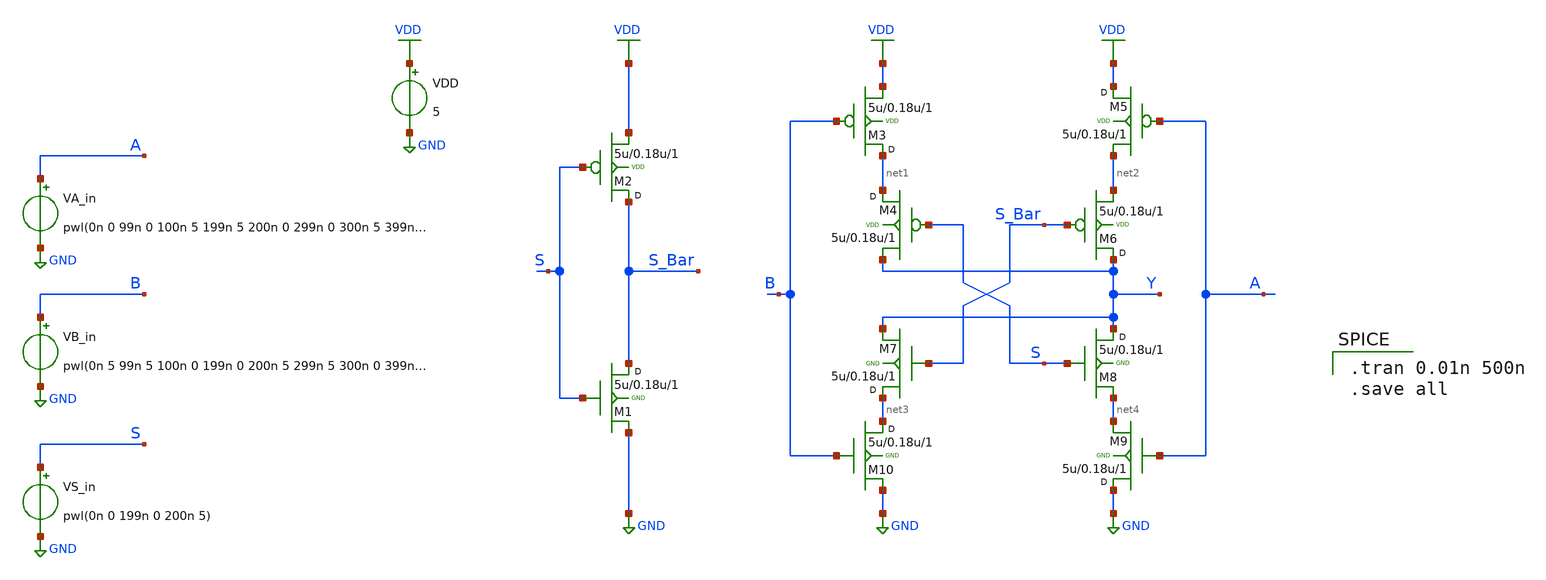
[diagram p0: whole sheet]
** sch_path: sch/MUX2X1_size_diff.sch
**.subckt MUX2X1_size_diff
M1 S_Bar S GND GND nfet w=5u l=0.18u m=1
M2 S_Bar S VDD VDD pfet w=5u l=0.18u m=1
M3 net1 B VDD VDD pfet w=5u l=0.18u m=1
M4 net1 S Y VDD pfet w=5u l=0.18u m=1
M5 VDD A net2 VDD pfet w=5u l=0.18u m=1
M6 Y S_Bar net2 VDD pfet w=5u l=0.18u m=1
M7 net3 S_Bar Y GND nfet w=5u l=0.18u m=1
M8 Y S net4 GND nfet w=5u l=0.18u m=1
M9 GND A net4 GND nfet w=5u l=0.18u m=1
M10 net3 B GND GND nfet w=5u l=0.18u m=1
VDD VDD GND 5
VA_in A GND pwl(0n 0 99n 0 100n 5 199n 5 200n 0 299n 0 300n 5 399n 5 400n 0)
VB_in B GND pwl(0n 5 99n 5 100n 0 199n 0 200n 5 299n 5 300n 0 399n 0 400n 5)
VS_in S GND pwl(0n 0 199n 0 200n 5)
**** begin user architecture code

.option wnflag=1
.MODEL nfet NMOS ( LEVEL   = 49 VERSION = 3.1            TNOM    = 27             TOX     = 1.4E-8
+ XJ      = 1.5E-7         NCH     = 1.7E17         VTH0    = 0.6484638 K1      = 0.8874212      K2
+      = -0.0978537     K3      = 24.0034885 K3B     = -7.2553705     W0      = 1.268969E-8    NLX     =
+ 1E-9 DVT0W   = 0              DVT1W   = 0              DVT2W   = 0 DVT0    = 3.8899304      DVT1    =
+ 0.4295545      DVT2    = -0.0862625 U0      = 454.7269155    UA      = 1E-13          UB      = 1.362113E-18
+ UC      = 1.430811E-11   VSAT    = 1.629926E5     A0      = 0.6165742 AGS     = 0.1163052      B0
+      = 2.433887E-6    B1      = 5E-6 KETA    = -2.051055E-3   A1      = 6.710587E-5    A2      = 0.37115
+ RDSW    = 1.342046E3     PRWG    = 0.0525473      PRWB    = 0.0422162 WR      = 1              WINT    =
+ 2.317656E-7    LINT    = 3.438422E-8 XL      = 0              XW      = 0              DWG     = -1.197811E-8
+ DWB     = 6.032429E-8    VOFF    = 0              NFACTOR = 0.684939 CIT     = 0              CDSC    =
+ 2.4E-4         CDSCD   = 0 CDSCB   = 0              ETA0    = 0.0323024      ETAB    = -1.472177E-3 DSUB
+    = 0.2796903      PCLM    = 2.5557332      PDIBLC1 = -0.2401157 PDIBLC2 = 2.505188E-3    PDIBLCB =
+ -0.0520225     DROUT   = 0.5945619 PSCBE1  = 5.499244E8     PSCBE2  = 4.527916E-5    PVAG    = 0 DELTA   =
+ 0.01           RSH     = 80.3           MOBMOD  = 1 PRT     = 0              UTE     = -1.5
+           KT1     = -0.11 KT1L    = 0              KT2     = 0.022          UA1     = 4.31E-9 UB1     = -7.61E-18
+      UC1     = -5.6E-11       AT      = 3.3E4 WL      = 0              WLN     = 1              WW      = 0
+ WWN     = 1              WWL     = 0              LL      = 0 LLN     = 1              LW      = 0
+              LWN     = 1 LWL     = 0              CAPMOD  = 2              XPART   = 0.5 CGDO    = 2.1E-10
+        CGSO    = 2.1E-10        CGBO    = 1E-9 CJ      = 4.156656E-4    PB      = 0.99           MJ      =
+ 0.4479288 CJSW    = 3.399348E-10   PBSW    = 0.1            MJSW    = 0.1142026 CJSWG   = 1.64E-10
+       PBSWG   = 0.1            MJSWG   = 0.1142026 CF      = 0              PVTH0   = 0.0959658      PRDSW   =
+ 103.9415756 PK2     = -0.034767      WKETA   = -0.0168116     LKETA   = 1.239789E-3     )


.MODEL pfet PMOS ( LEVEL   = 49 VERSION = 3.1            TNOM    = 27             TOX     = 1.4E-8
+ XJ      = 1.5E-7         NCH     = 1.7E17         VTH0    = -0.9500724 K1      = 0.5456507      K2
+      = 0.0105576      K3      = 4.5052654 K3B     = -0.931974      W0      = 1.127003E-7    NLX     =
+ 3.819935E-8 DVT0W   = 0              DVT1W   = 0              DVT2W   = 0 DVT0    = 2.7369297      DVT1    =
+ 0.4803414      DVT2    = -0.0786477 U0      = 212.1726489    UA      = 2.800492E-9    UB      = 1.059959E-21
+ UC      = -6.21265E-11   VSAT    = 2E5            A0      = 0.894794 AGS     = 0.1277092      B0
+      = 5.079049E-7    B1      = 5E-6 KETA    = -1.969136E-3   A1      = 0              A2      = 0.3 RDSW
+    = 2.51727E3      PRWG    = -3.93537E-3    PRWB    = -6.474415E-3 WR      = 1              WINT    =
+ 2.846891E-7    LINT    = 5.207504E-8 XL      = 0              XW      = 0              DWG     = -1.894994E-8
+ DWB     = 1.793161E-8    VOFF    = -0.0589646     NFACTOR = 0.9229882 CIT     = 0              CDSC
+    = 2.4E-4         CDSCD   = 0 CDSCB   = 0              ETA0    = 0.3701754      ETAB    = -0.0747353
+ DSUB    = 1              PCLM    = 2.0661973      PDIBLC1 = 0.0491197 PDIBLC2 = 4.022205E-3    PDIBLCB =
+ -0.0622551     DROUT   = 0.2243213 PSCBE1  = 5.126179E9     PSCBE2  = 5.004119E-10   PVAG    = 0.0167107 DELTA
+   = 0.01           RSH     = 101.7          MOBMOD  = 1 PRT     = 0              UTE     = -1.5
+           KT1     = -0.11 KT1L    = 0              KT2     = 0.022          UA1     = 4.31E-9 UB1     = -7.61E-18
+      UC1     = -5.6E-11       AT      = 3.3E4 WL      = 0              WLN     = 1              WW      = 0
+ WWN     = 1              WWL     = 0              LL      = 0 LLN     = 1              LW      = 0
+              LWN     = 1 LWL     = 0              CAPMOD  = 2              XPART   = 0.5 CGDO    = 2.89E-10
+       CGSO    = 2.89E-10       CGBO    = 1E-9 CJ      = 7.264536E-4    PB      = 0.9566163      MJ      =
+ 0.4977596 CJSW    = 2.873502E-10   PBSW    = 0.99           MJSW    = 0.3106308 CJSWG   = 6.4E-11
+        PBSWG   = 0.99           MJSWG   = 0.3106308 CF      = 0              PVTH0   = 5.98016E-3     PRDSW   =
+ 14.8598424 PK2     = 3.73981E-3     WKETA   = 3.685103E-3    LKETA   = -4.456587E-3    )
*



.tran 0.01n 500n
.save all

**** end user architecture code
**.ends
.GLOBAL GND
.GLOBAL VDD
.end
